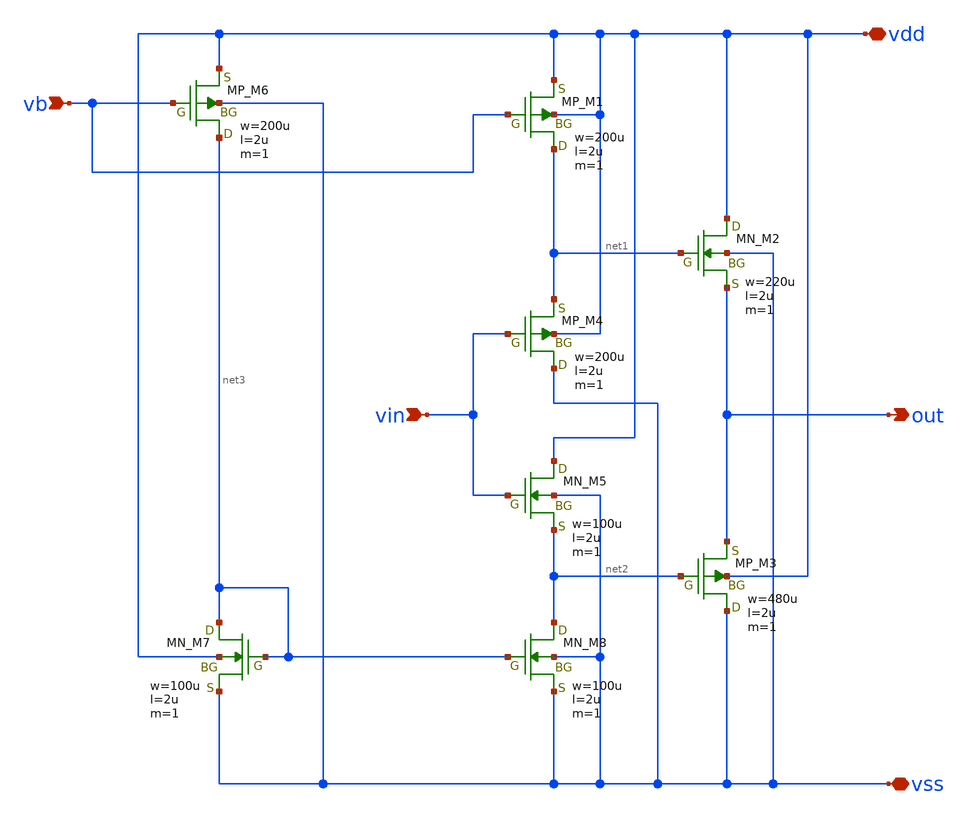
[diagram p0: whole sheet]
** sch_path: 555timer_bk/cs.sch
**.subckt cs vb vin out vss vdd
*.ipin vb
*.ipin vin
*.opin out
*.iopin vss
*.iopin vdd
XM6 net3 vb vdd vss PMOS w=200u l=2u as=0 ad=0 ps=0 pd=0 nrd=0 nrs=0 m=1
XM7 net3 net3 vss vdd NMOS w=100u l=2u as=0 ad=0 ps=0 pd=0 nrd=0 nrs=0 m=1
XM1 net1 vb vdd vdd PMOS w=200u l=2u as=0 ad=0 ps=0 pd=0 nrd=0 nrs=0 m=1
XM2 vdd net1 out vss NMOS w=220u l=2u as=0 ad=0 ps=0 pd=0 nrd=0 nrs=0 m=1
XM3 vss net2 out vdd PMOS w=480u l=2u as=0 ad=0 ps=0 pd=0 nrd=0 nrs=0 m=1
XM4 vss vin net1 vdd PMOS w=200u l=2u as=0 ad=0 ps=0 pd=0 nrd=0 nrs=0 m=1
XM5 vdd vin net2 vss NMOS w=100u l=2u as=0 ad=0 ps=0 pd=0 nrd=0 nrs=0 m=1
XM8 net2 net3 vss vss NMOS w=100u l=2u as=0 ad=0 ps=0 pd=0 nrd=0 nrs=0 m=1
**.ends
.end
